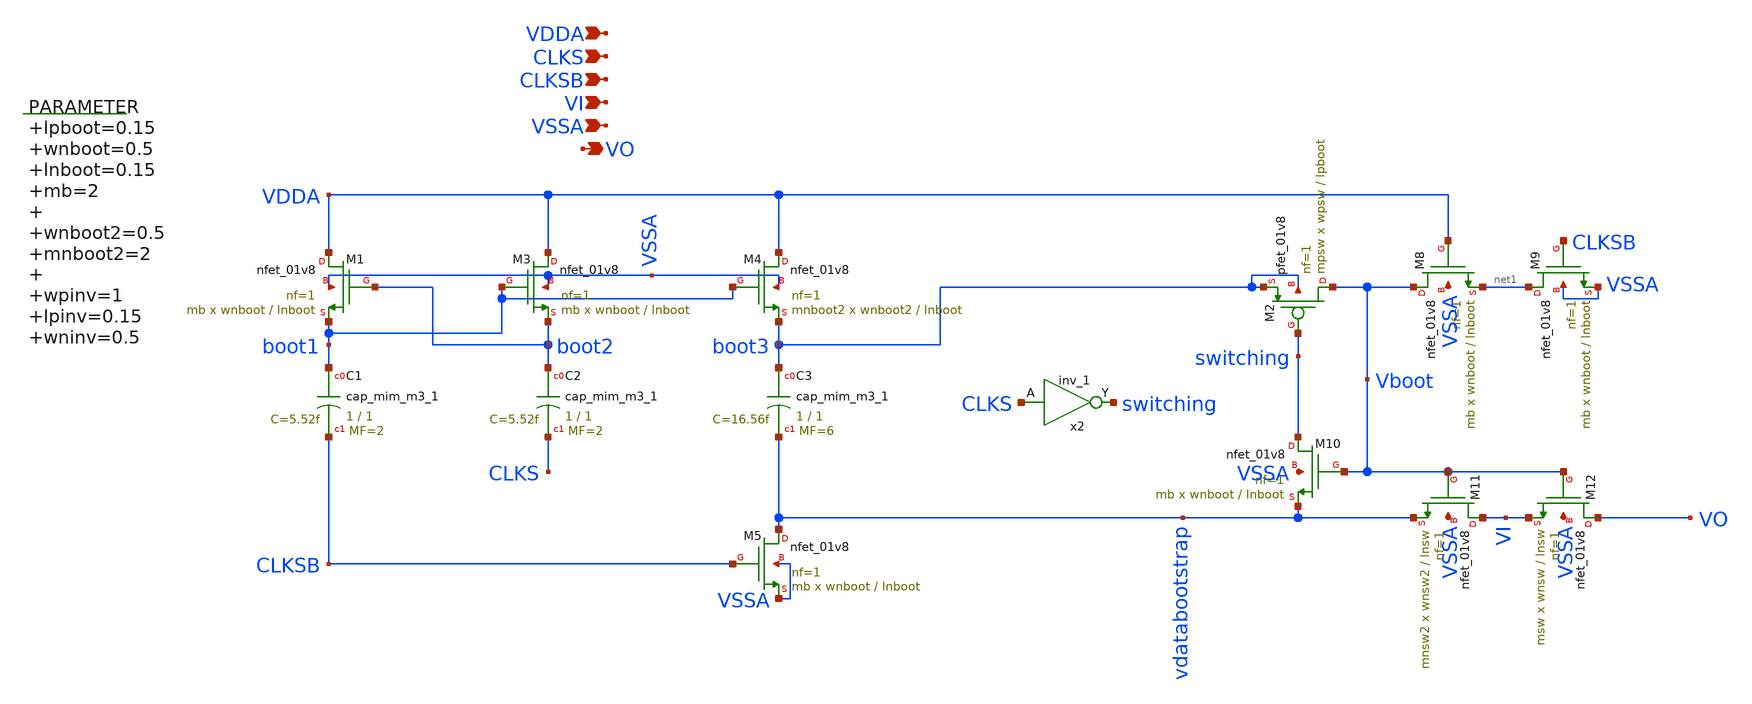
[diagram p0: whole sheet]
** sch_path: xschem/sh_bsw.sch
**.subckt sh_bsw VDDA CLKS CLKSB VI VSSA VO
*.ipin VDDA
*.ipin CLKS
*.ipin CLKSB
*.ipin VI
*.ipin VSSA
*.opin VO
.param lpboot=0.15 wnboot=0.5 lnboot=0.15 mb=2 wnboot2=0.5 mnboot2=2 wpinv=1 lpinv=0.15 wninv=0.5
+ lninv=0.15 wnsw=0.5 lnsw=0.3 msw=4 wnsw2=0.5 mnsw2=2 wpsw=0.5 mpsw=4
XM1 VDDA boot2 boot1 VSSA sky130_fd_pr__nfet_01v8 L=lnboot W=wnboot nf=1 ad='int((nf+1)/2) * W/nf * 0.29'
+ as='int((nf+2)/2) * W/nf * 0.29' pd='2*int((nf+1)/2) * (W/nf + 0.29)' ps='2*int((nf+2)/2) * (W/nf + 0.29)'
+ nrd='0.29 / W' nrs='0.29 / W' sa=0 sb=0 sd=0 mult=mb m=mb
XM2 Vboot switching boot3 boot3 sky130_fd_pr__pfet_01v8 L=lpboot W=wpsw nf=1 ad='int((nf+1)/2) * W/nf * 0.29'
+ as='int((nf+2)/2) * W/nf * 0.29' pd='2*int((nf+1)/2) * (W/nf + 0.29)' ps='2*int((nf+2)/2) * (W/nf + 0.29)'
+ nrd='0.29 / W' nrs='0.29 / W' sa=0 sb=0 sd=0 mult=mpsw m=mpsw
XC1 boot1 CLKSB sky130_fd_pr__cap_mim_m3_1 W=1 L=1 MF=2 m=2
XC2 boot2 CLKS sky130_fd_pr__cap_mim_m3_1 W=1 L=1 MF=2 m=2
XM4 VDDA boot1 boot3 VSSA sky130_fd_pr__nfet_01v8 L=lnboot W=wnboot2 nf=1 ad='int((nf+1)/2) * W/nf * 0.29'
+ as='int((nf+2)/2) * W/nf * 0.29' pd='2*int((nf+1)/2) * (W/nf + 0.29)' ps='2*int((nf+2)/2) * (W/nf + 0.29)'
+ nrd='0.29 / W' nrs='0.29 / W' sa=0 sb=0 sd=0 mult=mnboot2 m=mnboot2
XM5 vdatabootstrap CLKSB VSSA VSSA sky130_fd_pr__nfet_01v8 L=lnboot W=wnboot nf=1 ad='int((nf+1)/2) * W/nf * 0.29'
+ as='int((nf+2)/2) * W/nf * 0.29' pd='2*int((nf+1)/2) * (W/nf + 0.29)' ps='2*int((nf+2)/2) * (W/nf + 0.29)'
+ nrd='0.29 / W' nrs='0.29 / W' sa=0 sb=0 sd=0 mult=mb m=mb
XC3 boot3 vdatabootstrap sky130_fd_pr__cap_mim_m3_1 W=1 L=1 MF=6 m=6
XM8 Vboot VDDA net1 VSSA sky130_fd_pr__nfet_01v8 L=lnboot W=wnboot nf=1 ad='int((nf+1)/2) * W/nf * 0.29'
+ as='int((nf+2)/2) * W/nf * 0.29' pd='2*int((nf+1)/2) * (W/nf + 0.29)' ps='2*int((nf+2)/2) * (W/nf + 0.29)'
+ nrd='0.29 / W' nrs='0.29 / W' sa=0 sb=0 sd=0 mult=mb m=mb
XM9 net1 CLKSB VSSA VSSA sky130_fd_pr__nfet_01v8 L=lnboot W=wnboot nf=1 ad='int((nf+1)/2) * W/nf * 0.29'
+ as='int((nf+2)/2) * W/nf * 0.29' pd='2*int((nf+1)/2) * (W/nf + 0.29)' ps='2*int((nf+2)/2) * (W/nf + 0.29)'
+ nrd='0.29 / W' nrs='0.29 / W' sa=0 sb=0 sd=0 mult=mb m=mb
XM10 switching Vboot vdatabootstrap VSSA sky130_fd_pr__nfet_01v8 L=lnboot W=wnboot nf=1 ad='int((nf+1)/2) * W/nf * 0.29'
+ as='int((nf+2)/2) * W/nf * 0.29' pd='2*int((nf+1)/2) * (W/nf + 0.29)' ps='2*int((nf+2)/2) * (W/nf + 0.29)'
+ nrd='0.29 / W' nrs='0.29 / W' sa=0 sb=0 sd=0 mult=mb m=mb
XM11 VI Vboot vdatabootstrap VSSA sky130_fd_pr__nfet_01v8 L=lnsw W=wnsw2 nf=1 ad='int((nf+1)/2) * W/nf * 0.29'
+ as='int((nf+2)/2) * W/nf * 0.29' pd='2*int((nf+1)/2) * (W/nf + 0.29)' ps='2*int((nf+2)/2) * (W/nf + 0.29)'
+ nrd='0.29 / W' nrs='0.29 / W' sa=0 sb=0 sd=0 mult=mnsw2 m=mnsw2
XM12 VO Vboot VI VSSA sky130_fd_pr__nfet_01v8 L=lnsw W=wnsw nf=1 ad='int((nf+1)/2) * W/nf * 0.29' as='int((nf+2)/2) * W/nf * 0.29'
+ pd='2*int((nf+1)/2) * (W/nf + 0.29)' ps='2*int((nf+2)/2) * (W/nf + 0.29)' nrd='0.29 / W' nrs='0.29 / W'
+ sa=0 sb=0 sd=0 mult=msw m=msw
XM3 VDDA boot1 boot2 VSSA sky130_fd_pr__nfet_01v8 L=lnboot W=wnboot nf=1 ad='int((nf+1)/2) * W/nf * 0.29'
+ as='int((nf+2)/2) * W/nf * 0.29' pd='2*int((nf+1)/2) * (W/nf + 0.29)' ps='2*int((nf+2)/2) * (W/nf + 0.29)'
+ nrd='0.29 / W' nrs='0.29 / W' sa=0 sb=0 sd=0 mult=mb m=mb
x2 CLKS vdatabootstrap VSSA VDDA VDDA switching sky130_fd_sc_hd__inv_1
**.ends
.end
